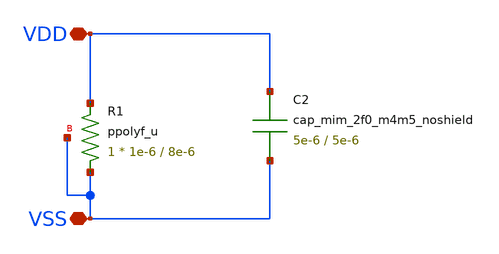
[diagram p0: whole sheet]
** sch_path: noritsuna/CDAC/Bo-Yu_Tseng/LVS/cdac_lvs.sch
* Copyright 2022 GlobalFoundries PDK Authors
* Licensed under the Apache License, Version 2.0 (the "License");
* you may not use this file except in compliance with the License.
* You may obtain a copy of the License at
* https://www.apache.org/licenses/LICENSE-2.0
* Unless required by applicable law or agreed to in writing, software
* distributed under the License is distributed on an "AS IS" BASIS,
* WITHOUT WARRANTIES OR CONDITIONS OF ANY KIND, either express or implied.
* See the License for the specific language governing permissions and
* limitations under the License.
**.subckt cdac_lvs VDD VSS
*.iopin VDD
*.iopin VSS
C2 VDD VSS cap_mim_2f0_m4m5_noshield W=5e-6 L=5e-6
R1 VSS VDD VSS ppolyf_u W=1e-6 L=8e-6 m=1
**.ends
.end
